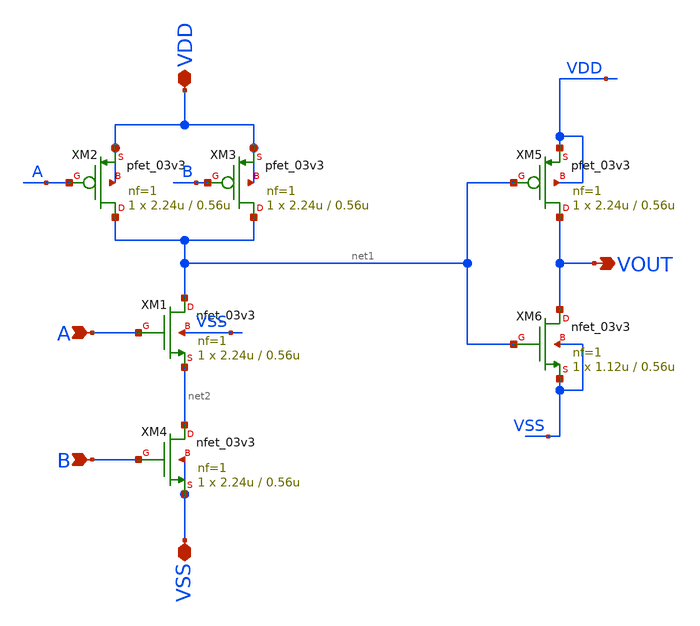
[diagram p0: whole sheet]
** sch_path: PLL-main/schematic/xschem/AND.sch
**.subckt AND VDD VSS A B VOUT
*.iopin VDD
*.iopin VSS
*.ipin A
*.ipin B
*.opin VOUT
XM1 net1 A net2 VSS nfet_03v3 L=0.56u W=2.24u nf=1 ad='int((nf+1)/2) * W/nf * 0.18u' as='int((nf+2)/2) * W/nf * 0.18u'
+ pd='2*int((nf+1)/2) * (W/nf + 0.18u)' ps='2*int((nf+2)/2) * (W/nf + 0.18u)' nrd='0.18u / W' nrs='0.18u / W'
+ sa=0 sb=0 sd=0 m=1
XM2 net1 A VDD VDD pfet_03v3 L=0.56u W=2.24u nf=1 ad='int((nf+1)/2) * W/nf * 0.18u' as='int((nf+2)/2) * W/nf * 0.18u'
+ pd='2*int((nf+1)/2) * (W/nf + 0.18u)' ps='2*int((nf+2)/2) * (W/nf + 0.18u)' nrd='0.18u / W' nrs='0.18u / W'
+ sa=0 sb=0 sd=0 m=1
XM3 net1 B VDD VDD pfet_03v3 L=0.56u W=2.24u nf=1 ad='int((nf+1)/2) * W/nf * 0.18u' as='int((nf+2)/2) * W/nf * 0.18u'
+ pd='2*int((nf+1)/2) * (W/nf + 0.18u)' ps='2*int((nf+2)/2) * (W/nf + 0.18u)' nrd='0.18u / W' nrs='0.18u / W'
+ sa=0 sb=0 sd=0 m=1
XM4 net2 B VSS VSS nfet_03v3 L=0.56u W=2.24u nf=1 ad='int((nf+1)/2) * W/nf * 0.18u' as='int((nf+2)/2) * W/nf * 0.18u'
+ pd='2*int((nf+1)/2) * (W/nf + 0.18u)' ps='2*int((nf+2)/2) * (W/nf + 0.18u)' nrd='0.18u / W' nrs='0.18u / W'
+ sa=0 sb=0 sd=0 m=1
XM5 VOUT net1 VDD VDD pfet_03v3 L=0.56u W=2.24u nf=1 ad='int((nf+1)/2) * W/nf * 0.18u' as='int((nf+2)/2) * W/nf * 0.18u'
+ pd='2*int((nf+1)/2) * (W/nf + 0.18u)' ps='2*int((nf+2)/2) * (W/nf + 0.18u)' nrd='0.18u / W' nrs='0.18u / W'
+ sa=0 sb=0 sd=0 m=1
XM6 VOUT net1 VSS VSS nfet_03v3 L=0.56u W=1.12u nf=1 ad='int((nf+1)/2) * W/nf * 0.18u' as='int((nf+2)/2) * W/nf * 0.18u'
+ pd='2*int((nf+1)/2) * (W/nf + 0.18u)' ps='2*int((nf+2)/2) * (W/nf + 0.18u)' nrd='0.18u / W' nrs='0.18u / W'
+ sa=0 sb=0 sd=0 m=1
**.ends
.end
